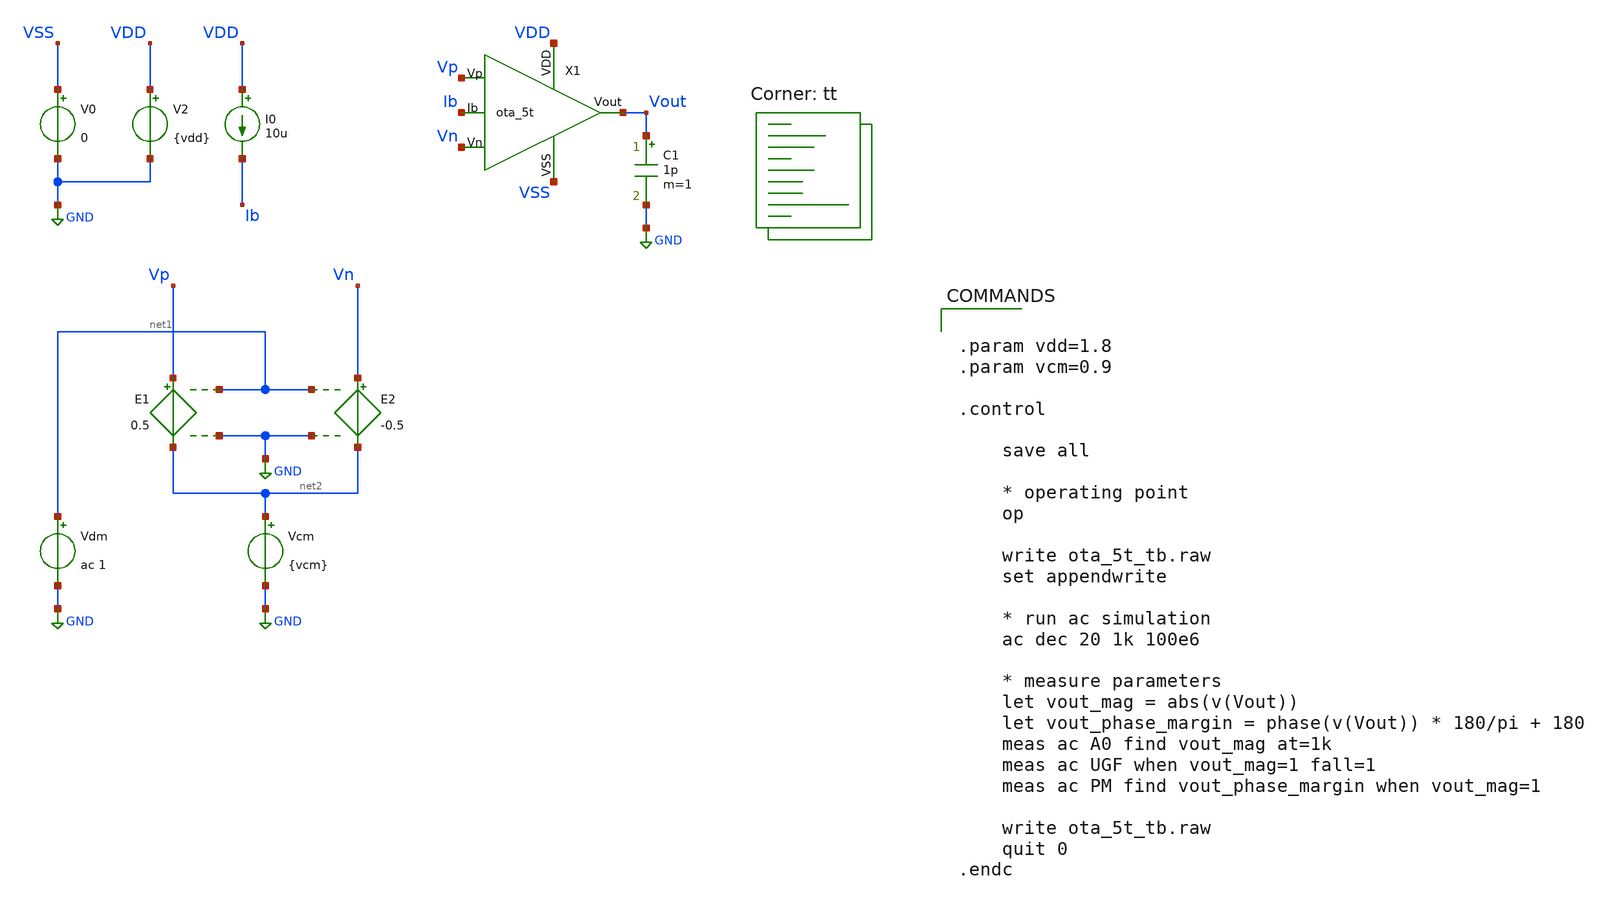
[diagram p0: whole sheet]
** sch_path: xschem/ota_5t_tb.sch
**.subckt ota_5t_tb
I0 VDD Ib 10u
C1 Vout GND 1p m=1
V0 VSS GND 0
V2 VDD GND {vdd}
E1 Vp net2 net1 GND 0.5
E2 Vn net2 net1 GND -0.5
Vdm net1 GND ac 1
Vcm net2 GND {vcm}
X1 Ib Vn Vp Vout VDD VSS ota_5t
**** begin user architecture code


.param vdd=1.8
.param vcm=0.9

.control

    save all

    * operating point
    op

    write ota_5t_tb.raw
    set appendwrite

    * run ac simulation
    ac dec 20 1k 100e6

    * measure parameters
    let vout_mag = abs(v(Vout))
    let vout_phase_margin = phase(v(Vout)) * 180/pi + 180
    meas ac A0 find vout_mag at=1k
    meas ac UGF when vout_mag=1 fall=1
    meas ac PM find vout_phase_margin when vout_mag=1

    write ota_5t_tb.raw
    quit 0
.endc


.lib $::SKYWATER_MODELS/sky130.lib.spice tt
**** end user architecture code
**.ends

* expanding   symbol:  /home/unixpoly/analog/projects/sky130/ota_5t/xschem/ota_5t.sym # of pins=6
** sym_path: xschem/ota_5t.sym
** sch_path: xschem/ota_5t.sch
.subckt ota_5t Ib Vn Vp Vout VDD VSS
*.iopin VDD
*.iopin VSS
*.opin Vout
*.ipin Vp
*.ipin Vn
*.ipin Ib
XM3 net2 Vp net1 VSS sky130_fd_pr__nfet_01v8 L=0.5 W=3 nf=1 ad='int((1 + 1)/2) * 3 / 1 * 0.29' as='int((1 + 2)/2) * 3 / 1 * 0.29'
+ pd='2*int((1 + 1)/2) * (3 / 1 + 0.29)' ps='2*int((1 + 2)/2) * (3 / 1 + 0.29)' nrd='0.29 / 3 ' nrs='0.29 / 3 '
+ sa=0 sb=0 sd=0 mult=1 m=1
XM1 net2 net2 VDD VDD sky130_fd_pr__pfet_01v8 L=1 W=4.5 nf=1 ad='int((nf+1)/2) * W/nf * 0.29' as='int((nf+2)/2) * W/nf * 0.29'
+ pd='2*int((nf+1)/2) * (W/nf + 0.29)' ps='2*int((nf+2)/2) * (W/nf + 0.29)' nrd='0.29 / W' nrs='0.29 / W'
+ sa=0 sb=0 sd=0 mult=1 m=1
XM2 Vout net2 VDD VDD sky130_fd_pr__pfet_01v8 L=1 W=4.5 nf=1 ad='int((nf+1)/2) * W/nf * 0.29' as='int((nf+2)/2) * W/nf * 0.29'
+ pd='2*int((nf+1)/2) * (W/nf + 0.29)' ps='2*int((nf+2)/2) * (W/nf + 0.29)' nrd='0.29 / W' nrs='0.29 / W'
+ sa=0 sb=0 sd=0 mult=1 m=1
XM4 Vout Vn net1 VSS sky130_fd_pr__nfet_01v8 L=0.5 W=3 nf=1 ad='int((1 + 1)/2) * 3 / 1 * 0.29' as='int((1 + 2)/2) * 3 / 1 * 0.29'
+ pd='2*int((1 + 1)/2) * (3 / 1 + 0.29)' ps='2*int((1 + 2)/2) * (3 / 1 + 0.29)' nrd='0.29 / 3 ' nrs='0.29 / 3 '
+ sa=0 sb=0 sd=0 mult=1 m=1
XM5 net1 Ib VSS VSS sky130_fd_pr__nfet_01v8 L=1 W=4 nf=1 ad='int((1 + 1)/2) * 4 / 1 * 0.29' as='int((1 + 2)/2) * 4 / 1 * 0.29'
+ pd='2*int((1 + 1)/2) * (4 / 1 + 0.29)' ps='2*int((1 + 2)/2) * (4 / 1 + 0.29)' nrd='0.29 / 4 ' nrs='0.29 / 4 '
+ sa=0 sb=0 sd=0 mult=1 m=1
XM6 Ib Ib VSS VSS sky130_fd_pr__nfet_01v8 L=1 W=4 nf=1 ad='int((1 + 1)/2) * 4 / 1 * 0.29' as='int((1 + 2)/2) * 4 / 1 * 0.29'
+ pd='2*int((1 + 1)/2) * (4 / 1 + 0.29)' ps='2*int((1 + 2)/2) * (4 / 1 + 0.29)' nrd='0.29 / 4 ' nrs='0.29 / 4 '
+ sa=0 sb=0 sd=0 mult=1 m=1
.ends

.GLOBAL GND
.end
